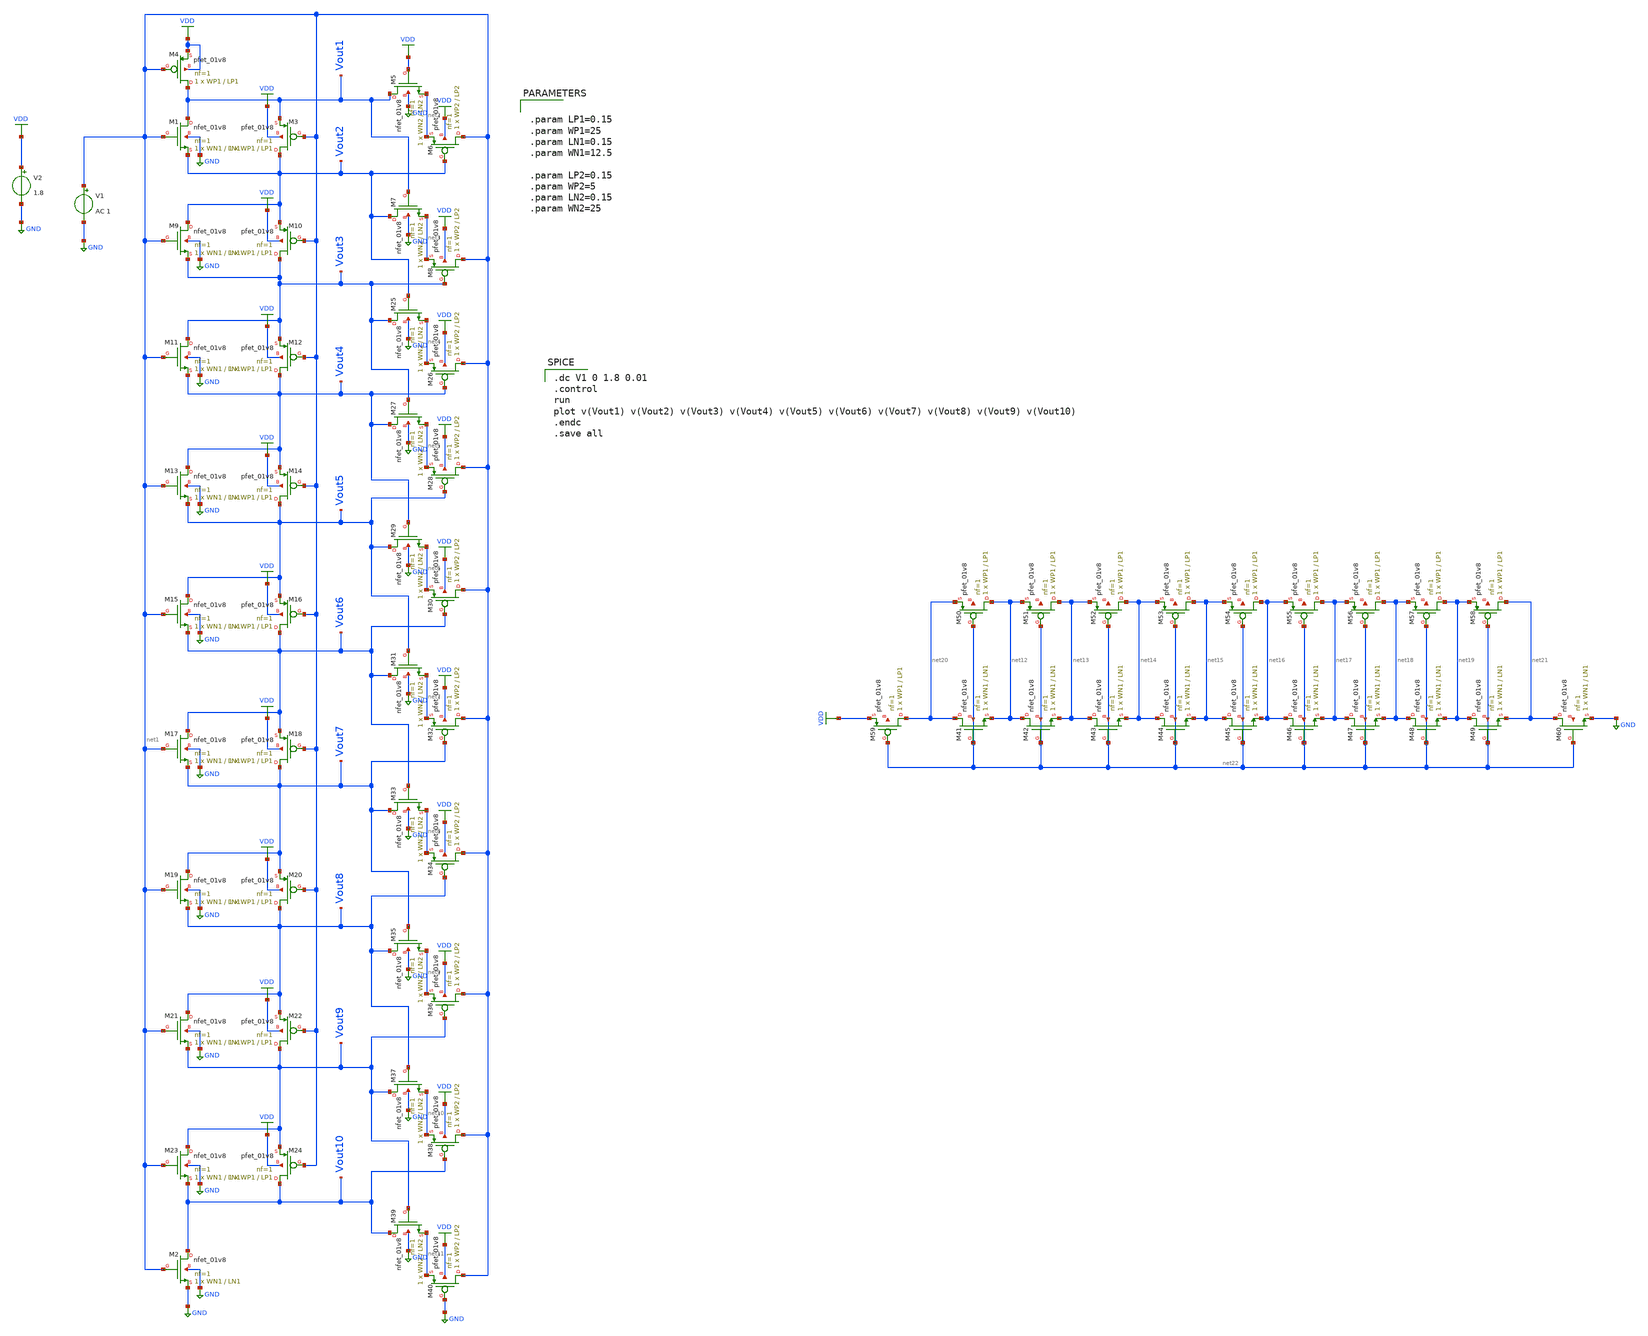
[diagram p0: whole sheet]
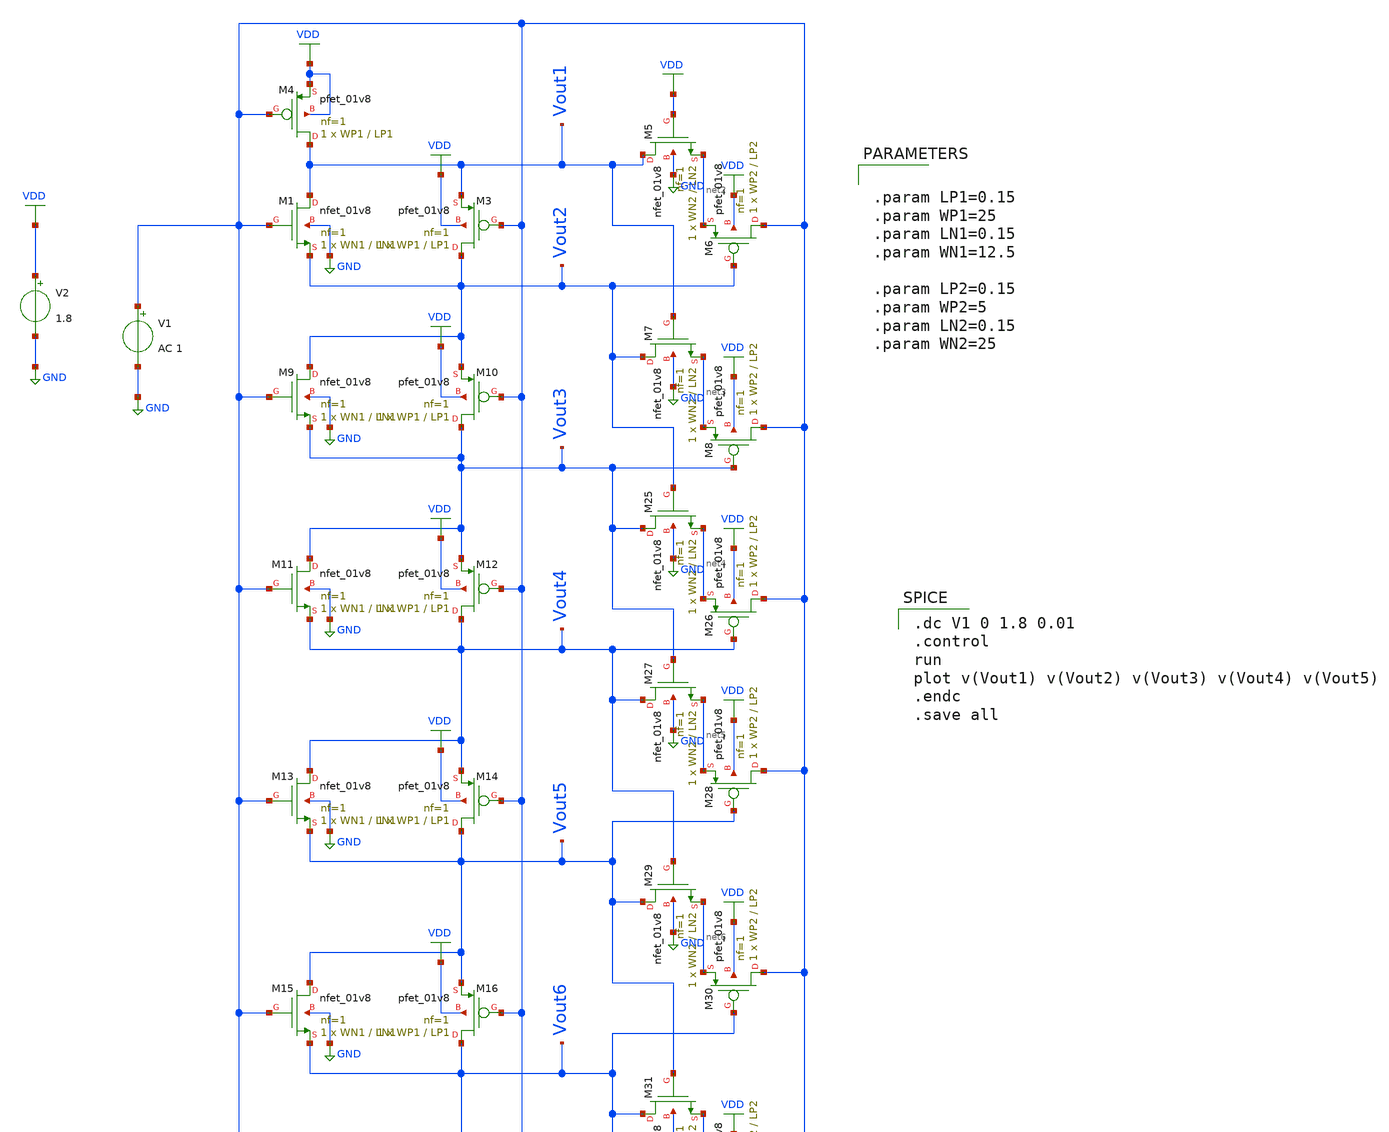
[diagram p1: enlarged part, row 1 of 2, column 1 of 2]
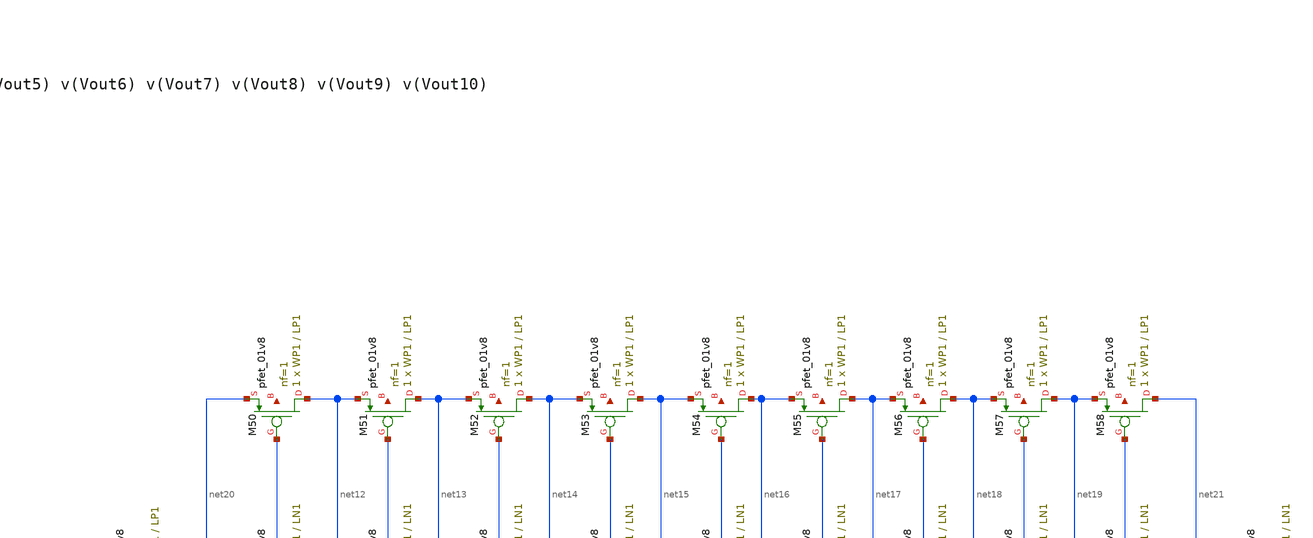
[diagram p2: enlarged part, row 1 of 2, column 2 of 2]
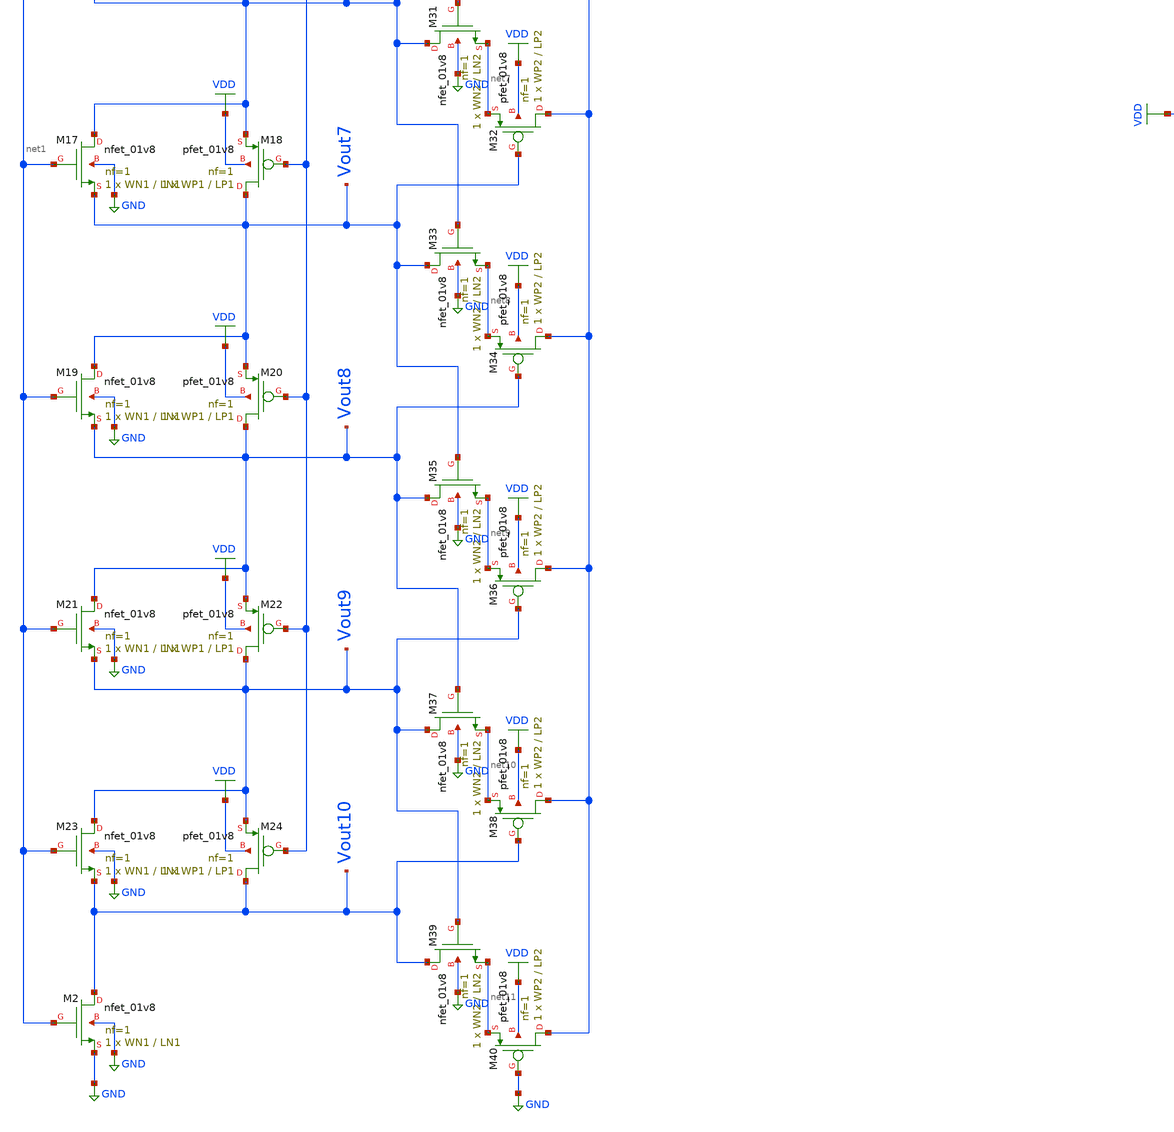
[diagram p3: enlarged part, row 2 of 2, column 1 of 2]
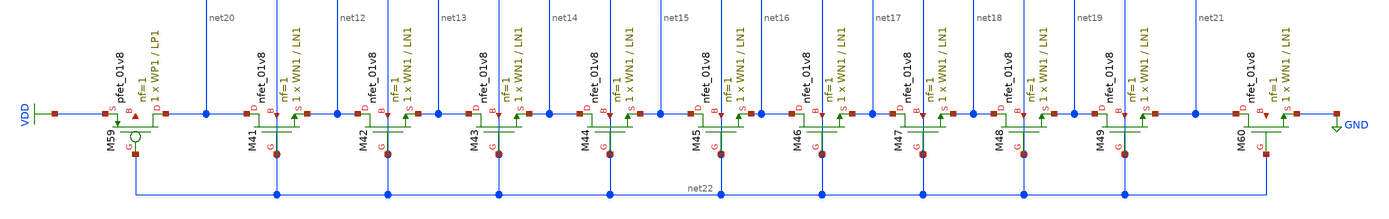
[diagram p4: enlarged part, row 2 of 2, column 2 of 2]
** sch_path: LIQAF circuit/10-Stage/10-stage LIQAF.sch
**.subckt 10-stage LIQAF
XM1 Vout1 net1 Vout2 GND sky130_fd_pr__nfet_01v8 L=LN1 W=WN1 nf=1 ad='int((nf+1)/2) * W/nf * 0.29' as='int((nf+2)/2) * W/nf * 0.29'
+ pd='2*int((nf+1)/2) * (W/nf + 0.29)' ps='2*int((nf+2)/2) * (W/nf + 0.29)' nrd='0.29 / W' nrs='0.29 / W'
+ sa=0 sb=0 sd=0 mult=1 m=1
V1 net1 GND AC 1
V2 VDD GND 1.8
XM2 Vout10 net1 GND GND sky130_fd_pr__nfet_01v8 L=LN1 W=WN1 nf=1 ad='int((nf+1)/2) * W/nf * 0.29' as='int((nf+2)/2) * W/nf * 0.29'
+ pd='2*int((nf+1)/2) * (W/nf + 0.29)' ps='2*int((nf+2)/2) * (W/nf + 0.29)' nrd='0.29 / W' nrs='0.29 / W'
+ sa=0 sb=0 sd=0 mult=1 m=1
XM3 Vout2 net1 Vout1 VDD sky130_fd_pr__pfet_01v8 L=LP1 W=WP1 nf=1 ad='int((nf+1)/2) * W/nf * 0.29' as='int((nf+2)/2) * W/nf * 0.29'
+ pd='2*int((nf+1)/2) * (W/nf + 0.29)' ps='2*int((nf+2)/2) * (W/nf + 0.29)' nrd='0.29 / W' nrs='0.29 / W'
+ sa=0 sb=0 sd=0 mult=1 m=1
XM4 Vout1 net1 VDD VDD sky130_fd_pr__pfet_01v8 L=LP1 W=WP1 nf=1 ad='int((nf+1)/2) * W/nf * 0.29' as='int((nf+2)/2) * W/nf * 0.29'
+ pd='2*int((nf+1)/2) * (W/nf + 0.29)' ps='2*int((nf+2)/2) * (W/nf + 0.29)' nrd='0.29 / W' nrs='0.29 / W'
+ sa=0 sb=0 sd=0 mult=1 m=1
XM5 Vout1 VDD net2 GND sky130_fd_pr__nfet_01v8 L=LN2 W=WN2 nf=1 ad='int((nf+1)/2) * W/nf * 0.29' as='int((nf+2)/2) * W/nf * 0.29'
+ pd='2*int((nf+1)/2) * (W/nf + 0.29)' ps='2*int((nf+2)/2) * (W/nf + 0.29)' nrd='0.29 / W' nrs='0.29 / W'
+ sa=0 sb=0 sd=0 mult=1 m=1
XM6 net1 Vout2 net2 VDD sky130_fd_pr__pfet_01v8 L=LP2 W=WP2 nf=1 ad='int((nf+1)/2) * W/nf * 0.29' as='int((nf+2)/2) * W/nf * 0.29'
+ pd='2*int((nf+1)/2) * (W/nf + 0.29)' ps='2*int((nf+2)/2) * (W/nf + 0.29)' nrd='0.29 / W' nrs='0.29 / W'
+ sa=0 sb=0 sd=0 mult=1 m=1
XM7 Vout2 Vout1 net3 GND sky130_fd_pr__nfet_01v8 L=LN2 W=WN2 nf=1 ad='int((nf+1)/2) * W/nf * 0.29' as='int((nf+2)/2) * W/nf * 0.29'
+ pd='2*int((nf+1)/2) * (W/nf + 0.29)' ps='2*int((nf+2)/2) * (W/nf + 0.29)' nrd='0.29 / W' nrs='0.29 / W'
+ sa=0 sb=0 sd=0 mult=1 m=1
XM8 net1 Vout3 net3 VDD sky130_fd_pr__pfet_01v8 L=LP2 W=WP2 nf=1 ad='int((nf+1)/2) * W/nf * 0.29' as='int((nf+2)/2) * W/nf * 0.29'
+ pd='2*int((nf+1)/2) * (W/nf + 0.29)' ps='2*int((nf+2)/2) * (W/nf + 0.29)' nrd='0.29 / W' nrs='0.29 / W'
+ sa=0 sb=0 sd=0 mult=1 m=1
XM9 Vout2 net1 Vout3 GND sky130_fd_pr__nfet_01v8 L=LN1 W=WN1 nf=1 ad='int((nf+1)/2) * W/nf * 0.29' as='int((nf+2)/2) * W/nf * 0.29'
+ pd='2*int((nf+1)/2) * (W/nf + 0.29)' ps='2*int((nf+2)/2) * (W/nf + 0.29)' nrd='0.29 / W' nrs='0.29 / W'
+ sa=0 sb=0 sd=0 mult=1 m=1
XM10 Vout3 net1 Vout2 VDD sky130_fd_pr__pfet_01v8 L=LP1 W=WP1 nf=1 ad='int((nf+1)/2) * W/nf * 0.29' as='int((nf+2)/2) * W/nf * 0.29'
+ pd='2*int((nf+1)/2) * (W/nf + 0.29)' ps='2*int((nf+2)/2) * (W/nf + 0.29)' nrd='0.29 / W' nrs='0.29 / W'
+ sa=0 sb=0 sd=0 mult=1 m=1
XM11 Vout3 net1 Vout4 GND sky130_fd_pr__nfet_01v8 L=LN1 W=WN1 nf=1 ad='int((nf+1)/2) * W/nf * 0.29' as='int((nf+2)/2) * W/nf * 0.29'
+ pd='2*int((nf+1)/2) * (W/nf + 0.29)' ps='2*int((nf+2)/2) * (W/nf + 0.29)' nrd='0.29 / W' nrs='0.29 / W'
+ sa=0 sb=0 sd=0 mult=1 m=1
XM12 Vout4 net1 Vout3 VDD sky130_fd_pr__pfet_01v8 L=LP1 W=WP1 nf=1 ad='int((nf+1)/2) * W/nf * 0.29' as='int((nf+2)/2) * W/nf * 0.29'
+ pd='2*int((nf+1)/2) * (W/nf + 0.29)' ps='2*int((nf+2)/2) * (W/nf + 0.29)' nrd='0.29 / W' nrs='0.29 / W'
+ sa=0 sb=0 sd=0 mult=1 m=1
XM13 Vout4 net1 Vout5 GND sky130_fd_pr__nfet_01v8 L=LN1 W=WN1 nf=1 ad='int((nf+1)/2) * W/nf * 0.29' as='int((nf+2)/2) * W/nf * 0.29'
+ pd='2*int((nf+1)/2) * (W/nf + 0.29)' ps='2*int((nf+2)/2) * (W/nf + 0.29)' nrd='0.29 / W' nrs='0.29 / W'
+ sa=0 sb=0 sd=0 mult=1 m=1
XM14 Vout5 net1 Vout4 VDD sky130_fd_pr__pfet_01v8 L=LP1 W=WP1 nf=1 ad='int((nf+1)/2) * W/nf * 0.29' as='int((nf+2)/2) * W/nf * 0.29'
+ pd='2*int((nf+1)/2) * (W/nf + 0.29)' ps='2*int((nf+2)/2) * (W/nf + 0.29)' nrd='0.29 / W' nrs='0.29 / W'
+ sa=0 sb=0 sd=0 mult=1 m=1
XM15 Vout5 net1 Vout6 GND sky130_fd_pr__nfet_01v8 L=LN1 W=WN1 nf=1 ad='int((nf+1)/2) * W/nf * 0.29' as='int((nf+2)/2) * W/nf * 0.29'
+ pd='2*int((nf+1)/2) * (W/nf + 0.29)' ps='2*int((nf+2)/2) * (W/nf + 0.29)' nrd='0.29 / W' nrs='0.29 / W'
+ sa=0 sb=0 sd=0 mult=1 m=1
XM16 Vout6 net1 Vout5 VDD sky130_fd_pr__pfet_01v8 L=LP1 W=WP1 nf=1 ad='int((nf+1)/2) * W/nf * 0.29' as='int((nf+2)/2) * W/nf * 0.29'
+ pd='2*int((nf+1)/2) * (W/nf + 0.29)' ps='2*int((nf+2)/2) * (W/nf + 0.29)' nrd='0.29 / W' nrs='0.29 / W'
+ sa=0 sb=0 sd=0 mult=1 m=1
XM17 Vout6 net1 Vout7 GND sky130_fd_pr__nfet_01v8 L=LN1 W=WN1 nf=1 ad='int((nf+1)/2) * W/nf * 0.29' as='int((nf+2)/2) * W/nf * 0.29'
+ pd='2*int((nf+1)/2) * (W/nf + 0.29)' ps='2*int((nf+2)/2) * (W/nf + 0.29)' nrd='0.29 / W' nrs='0.29 / W'
+ sa=0 sb=0 sd=0 mult=1 m=1
XM18 Vout7 net1 Vout6 VDD sky130_fd_pr__pfet_01v8 L=LP1 W=WP1 nf=1 ad='int((nf+1)/2) * W/nf * 0.29' as='int((nf+2)/2) * W/nf * 0.29'
+ pd='2*int((nf+1)/2) * (W/nf + 0.29)' ps='2*int((nf+2)/2) * (W/nf + 0.29)' nrd='0.29 / W' nrs='0.29 / W'
+ sa=0 sb=0 sd=0 mult=1 m=1
XM19 Vout7 net1 Vout8 GND sky130_fd_pr__nfet_01v8 L=LN1 W=WN1 nf=1 ad='int((nf+1)/2) * W/nf * 0.29' as='int((nf+2)/2) * W/nf * 0.29'
+ pd='2*int((nf+1)/2) * (W/nf + 0.29)' ps='2*int((nf+2)/2) * (W/nf + 0.29)' nrd='0.29 / W' nrs='0.29 / W'
+ sa=0 sb=0 sd=0 mult=1 m=1
XM20 Vout8 net1 Vout7 VDD sky130_fd_pr__pfet_01v8 L=LP1 W=WP1 nf=1 ad='int((nf+1)/2) * W/nf * 0.29' as='int((nf+2)/2) * W/nf * 0.29'
+ pd='2*int((nf+1)/2) * (W/nf + 0.29)' ps='2*int((nf+2)/2) * (W/nf + 0.29)' nrd='0.29 / W' nrs='0.29 / W'
+ sa=0 sb=0 sd=0 mult=1 m=1
XM21 Vout8 net1 Vout9 GND sky130_fd_pr__nfet_01v8 L=LN1 W=WN1 nf=1 ad='int((nf+1)/2) * W/nf * 0.29' as='int((nf+2)/2) * W/nf * 0.29'
+ pd='2*int((nf+1)/2) * (W/nf + 0.29)' ps='2*int((nf+2)/2) * (W/nf + 0.29)' nrd='0.29 / W' nrs='0.29 / W'
+ sa=0 sb=0 sd=0 mult=1 m=1
XM22 Vout9 net1 Vout8 VDD sky130_fd_pr__pfet_01v8 L=LP1 W=WP1 nf=1 ad='int((nf+1)/2) * W/nf * 0.29' as='int((nf+2)/2) * W/nf * 0.29'
+ pd='2*int((nf+1)/2) * (W/nf + 0.29)' ps='2*int((nf+2)/2) * (W/nf + 0.29)' nrd='0.29 / W' nrs='0.29 / W'
+ sa=0 sb=0 sd=0 mult=1 m=1
XM23 Vout9 net1 Vout10 GND sky130_fd_pr__nfet_01v8 L=LN1 W=WN1 nf=1 ad='int((nf+1)/2) * W/nf * 0.29'
+ as='int((nf+2)/2) * W/nf * 0.29' pd='2*int((nf+1)/2) * (W/nf + 0.29)' ps='2*int((nf+2)/2) * (W/nf + 0.29)'
+ nrd='0.29 / W' nrs='0.29 / W' sa=0 sb=0 sd=0 mult=1 m=1
XM24 Vout10 net1 Vout9 VDD sky130_fd_pr__pfet_01v8 L=LP1 W=WP1 nf=1 ad='int((nf+1)/2) * W/nf * 0.29'
+ as='int((nf+2)/2) * W/nf * 0.29' pd='2*int((nf+1)/2) * (W/nf + 0.29)' ps='2*int((nf+2)/2) * (W/nf + 0.29)'
+ nrd='0.29 / W' nrs='0.29 / W' sa=0 sb=0 sd=0 mult=1 m=1
XM25 Vout3 Vout2 net4 GND sky130_fd_pr__nfet_01v8 L=LN2 W=WN2 nf=1 ad='int((nf+1)/2) * W/nf * 0.29' as='int((nf+2)/2) * W/nf * 0.29'
+ pd='2*int((nf+1)/2) * (W/nf + 0.29)' ps='2*int((nf+2)/2) * (W/nf + 0.29)' nrd='0.29 / W' nrs='0.29 / W'
+ sa=0 sb=0 sd=0 mult=1 m=1
XM26 net1 Vout4 net4 VDD sky130_fd_pr__pfet_01v8 L=LP2 W=WP2 nf=1 ad='int((nf+1)/2) * W/nf * 0.29' as='int((nf+2)/2) * W/nf * 0.29'
+ pd='2*int((nf+1)/2) * (W/nf + 0.29)' ps='2*int((nf+2)/2) * (W/nf + 0.29)' nrd='0.29 / W' nrs='0.29 / W'
+ sa=0 sb=0 sd=0 mult=1 m=1
XM27 Vout4 Vout3 net5 GND sky130_fd_pr__nfet_01v8 L=LN2 W=WN2 nf=1 ad='int((nf+1)/2) * W/nf * 0.29' as='int((nf+2)/2) * W/nf * 0.29'
+ pd='2*int((nf+1)/2) * (W/nf + 0.29)' ps='2*int((nf+2)/2) * (W/nf + 0.29)' nrd='0.29 / W' nrs='0.29 / W'
+ sa=0 sb=0 sd=0 mult=1 m=1
XM28 net1 Vout5 net5 VDD sky130_fd_pr__pfet_01v8 L=LP2 W=WP2 nf=1 ad='int((nf+1)/2) * W/nf * 0.29' as='int((nf+2)/2) * W/nf * 0.29'
+ pd='2*int((nf+1)/2) * (W/nf + 0.29)' ps='2*int((nf+2)/2) * (W/nf + 0.29)' nrd='0.29 / W' nrs='0.29 / W'
+ sa=0 sb=0 sd=0 mult=1 m=1
XM29 Vout5 Vout4 net6 GND sky130_fd_pr__nfet_01v8 L=LN2 W=WN2 nf=1 ad='int((nf+1)/2) * W/nf * 0.29' as='int((nf+2)/2) * W/nf * 0.29'
+ pd='2*int((nf+1)/2) * (W/nf + 0.29)' ps='2*int((nf+2)/2) * (W/nf + 0.29)' nrd='0.29 / W' nrs='0.29 / W'
+ sa=0 sb=0 sd=0 mult=1 m=1
XM30 net1 Vout6 net6 VDD sky130_fd_pr__pfet_01v8 L=LP2 W=WP2 nf=1 ad='int((nf+1)/2) * W/nf * 0.29' as='int((nf+2)/2) * W/nf * 0.29'
+ pd='2*int((nf+1)/2) * (W/nf + 0.29)' ps='2*int((nf+2)/2) * (W/nf + 0.29)' nrd='0.29 / W' nrs='0.29 / W'
+ sa=0 sb=0 sd=0 mult=1 m=1
XM31 Vout6 Vout5 net7 GND sky130_fd_pr__nfet_01v8 L=LN2 W=WN2 nf=1 ad='int((nf+1)/2) * W/nf * 0.29' as='int((nf+2)/2) * W/nf * 0.29'
+ pd='2*int((nf+1)/2) * (W/nf + 0.29)' ps='2*int((nf+2)/2) * (W/nf + 0.29)' nrd='0.29 / W' nrs='0.29 / W'
+ sa=0 sb=0 sd=0 mult=1 m=1
XM32 net1 Vout7 net7 VDD sky130_fd_pr__pfet_01v8 L=LP2 W=WP2 nf=1 ad='int((nf+1)/2) * W/nf * 0.29' as='int((nf+2)/2) * W/nf * 0.29'
+ pd='2*int((nf+1)/2) * (W/nf + 0.29)' ps='2*int((nf+2)/2) * (W/nf + 0.29)' nrd='0.29 / W' nrs='0.29 / W'
+ sa=0 sb=0 sd=0 mult=1 m=1
XM33 Vout7 Vout6 net8 GND sky130_fd_pr__nfet_01v8 L=LN2 W=WN2 nf=1 ad='int((nf+1)/2) * W/nf * 0.29' as='int((nf+2)/2) * W/nf * 0.29'
+ pd='2*int((nf+1)/2) * (W/nf + 0.29)' ps='2*int((nf+2)/2) * (W/nf + 0.29)' nrd='0.29 / W' nrs='0.29 / W'
+ sa=0 sb=0 sd=0 mult=1 m=1
XM34 net1 Vout8 net8 VDD sky130_fd_pr__pfet_01v8 L=LP2 W=WP2 nf=1 ad='int((nf+1)/2) * W/nf * 0.29' as='int((nf+2)/2) * W/nf * 0.29'
+ pd='2*int((nf+1)/2) * (W/nf + 0.29)' ps='2*int((nf+2)/2) * (W/nf + 0.29)' nrd='0.29 / W' nrs='0.29 / W'
+ sa=0 sb=0 sd=0 mult=1 m=1
XM35 Vout8 Vout7 net9 GND sky130_fd_pr__nfet_01v8 L=LN2 W=WN2 nf=1 ad='int((nf+1)/2) * W/nf * 0.29' as='int((nf+2)/2) * W/nf * 0.29'
+ pd='2*int((nf+1)/2) * (W/nf + 0.29)' ps='2*int((nf+2)/2) * (W/nf + 0.29)' nrd='0.29 / W' nrs='0.29 / W'
+ sa=0 sb=0 sd=0 mult=1 m=1
XM36 net1 Vout9 net9 VDD sky130_fd_pr__pfet_01v8 L=LP2 W=WP2 nf=1 ad='int((nf+1)/2) * W/nf * 0.29' as='int((nf+2)/2) * W/nf * 0.29'
+ pd='2*int((nf+1)/2) * (W/nf + 0.29)' ps='2*int((nf+2)/2) * (W/nf + 0.29)' nrd='0.29 / W' nrs='0.29 / W'
+ sa=0 sb=0 sd=0 mult=1 m=1
XM37 Vout9 Vout8 net10 GND sky130_fd_pr__nfet_01v8 L=LN2 W=WN2 nf=1 ad='int((nf+1)/2) * W/nf * 0.29'
+ as='int((nf+2)/2) * W/nf * 0.29' pd='2*int((nf+1)/2) * (W/nf + 0.29)' ps='2*int((nf+2)/2) * (W/nf + 0.29)'
+ nrd='0.29 / W' nrs='0.29 / W' sa=0 sb=0 sd=0 mult=1 m=1
XM38 net1 Vout10 net10 VDD sky130_fd_pr__pfet_01v8 L=LP2 W=WP2 nf=1 ad='int((nf+1)/2) * W/nf * 0.29'
+ as='int((nf+2)/2) * W/nf * 0.29' pd='2*int((nf+1)/2) * (W/nf + 0.29)' ps='2*int((nf+2)/2) * (W/nf + 0.29)'
+ nrd='0.29 / W' nrs='0.29 / W' sa=0 sb=0 sd=0 mult=1 m=1
XM39 Vout10 Vout9 net11 GND sky130_fd_pr__nfet_01v8 L=LN2 W=WN2 nf=1 ad='int((nf+1)/2) * W/nf * 0.29'
+ as='int((nf+2)/2) * W/nf * 0.29' pd='2*int((nf+1)/2) * (W/nf + 0.29)' ps='2*int((nf+2)/2) * (W/nf + 0.29)'
+ nrd='0.29 / W' nrs='0.29 / W' sa=0 sb=0 sd=0 mult=1 m=1
XM40 net1 GND net11 VDD sky130_fd_pr__pfet_01v8 L=LP2 W=WP2 nf=1 ad='int((nf+1)/2) * W/nf * 0.29' as='int((nf+2)/2) * W/nf * 0.29'
+ pd='2*int((nf+1)/2) * (W/nf + 0.29)' ps='2*int((nf+2)/2) * (W/nf + 0.29)' nrd='0.29 / W' nrs='0.29 / W'
+ sa=0 sb=0 sd=0 mult=1 m=1
XM41 net20 net22 net12 net22 sky130_fd_pr__nfet_01v8 L=LN1 W=WN1 nf=1 ad='int((nf+1)/2) * W/nf * 0.29'
+ as='int((nf+2)/2) * W/nf * 0.29' pd='2*int((nf+1)/2) * (W/nf + 0.29)' ps='2*int((nf+2)/2) * (W/nf + 0.29)'
+ nrd='0.29 / W' nrs='0.29 / W' sa=0 sb=0 sd=0 mult=1 m=1
XM42 net12 net22 net13 net22 sky130_fd_pr__nfet_01v8 L=LN1 W=WN1 nf=1 ad='int((nf+1)/2) * W/nf * 0.29'
+ as='int((nf+2)/2) * W/nf * 0.29' pd='2*int((nf+1)/2) * (W/nf + 0.29)' ps='2*int((nf+2)/2) * (W/nf + 0.29)'
+ nrd='0.29 / W' nrs='0.29 / W' sa=0 sb=0 sd=0 mult=1 m=1
XM43 net13 net22 net14 net22 sky130_fd_pr__nfet_01v8 L=LN1 W=WN1 nf=1 ad='int((nf+1)/2) * W/nf * 0.29'
+ as='int((nf+2)/2) * W/nf * 0.29' pd='2*int((nf+1)/2) * (W/nf + 0.29)' ps='2*int((nf+2)/2) * (W/nf + 0.29)'
+ nrd='0.29 / W' nrs='0.29 / W' sa=0 sb=0 sd=0 mult=1 m=1
XM44 net14 net22 net15 net22 sky130_fd_pr__nfet_01v8 L=LN1 W=WN1 nf=1 ad='int((nf+1)/2) * W/nf * 0.29'
+ as='int((nf+2)/2) * W/nf * 0.29' pd='2*int((nf+1)/2) * (W/nf + 0.29)' ps='2*int((nf+2)/2) * (W/nf + 0.29)'
+ nrd='0.29 / W' nrs='0.29 / W' sa=0 sb=0 sd=0 mult=1 m=1
XM45 net15 net22 net16 net22 sky130_fd_pr__nfet_01v8 L=LN1 W=WN1 nf=1 ad='int((nf+1)/2) * W/nf * 0.29'
+ as='int((nf+2)/2) * W/nf * 0.29' pd='2*int((nf+1)/2) * (W/nf + 0.29)' ps='2*int((nf+2)/2) * (W/nf + 0.29)'
+ nrd='0.29 / W' nrs='0.29 / W' sa=0 sb=0 sd=0 mult=1 m=1
XM46 net16 net22 net17 net22 sky130_fd_pr__nfet_01v8 L=LN1 W=WN1 nf=1 ad='int((nf+1)/2) * W/nf * 0.29'
+ as='int((nf+2)/2) * W/nf * 0.29' pd='2*int((nf+1)/2) * (W/nf + 0.29)' ps='2*int((nf+2)/2) * (W/nf + 0.29)'
+ nrd='0.29 / W' nrs='0.29 / W' sa=0 sb=0 sd=0 mult=1 m=1
XM47 net17 net22 net18 net22 sky130_fd_pr__nfet_01v8 L=LN1 W=WN1 nf=1 ad='int((nf+1)/2) * W/nf * 0.29'
+ as='int((nf+2)/2) * W/nf * 0.29' pd='2*int((nf+1)/2) * (W/nf + 0.29)' ps='2*int((nf+2)/2) * (W/nf + 0.29)'
+ nrd='0.29 / W' nrs='0.29 / W' sa=0 sb=0 sd=0 mult=1 m=1
XM48 net18 net22 net19 net22 sky130_fd_pr__nfet_01v8 L=LN1 W=WN1 nf=1 ad='int((nf+1)/2) * W/nf * 0.29'
+ as='int((nf+2)/2) * W/nf * 0.29' pd='2*int((nf+1)/2) * (W/nf + 0.29)' ps='2*int((nf+2)/2) * (W/nf + 0.29)'
+ nrd='0.29 / W' nrs='0.29 / W' sa=0 sb=0 sd=0 mult=1 m=1
XM49 net19 net22 net21 net22 sky130_fd_pr__nfet_01v8 L=LN1 W=WN1 nf=1 ad='int((nf+1)/2) * W/nf * 0.29'
+ as='int((nf+2)/2) * W/nf * 0.29' pd='2*int((nf+1)/2) * (W/nf + 0.29)' ps='2*int((nf+2)/2) * (W/nf + 0.29)'
+ nrd='0.29 / W' nrs='0.29 / W' sa=0 sb=0 sd=0 mult=1 m=1
XM50 net12 net22 net20 net23 sky130_fd_pr__pfet_01v8 L=LP1 W=WP1 nf=1 ad='int((nf+1)/2) * W/nf * 0.29'
+ as='int((nf+2)/2) * W/nf * 0.29' pd='2*int((nf+1)/2) * (W/nf + 0.29)' ps='2*int((nf+2)/2) * (W/nf + 0.29)'
+ nrd='0.29 / W' nrs='0.29 / W' sa=0 sb=0 sd=0 mult=1 m=1
XM51 net13 net22 net12 net24 sky130_fd_pr__pfet_01v8 L=LP1 W=WP1 nf=1 ad='int((nf+1)/2) * W/nf * 0.29'
+ as='int((nf+2)/2) * W/nf * 0.29' pd='2*int((nf+1)/2) * (W/nf + 0.29)' ps='2*int((nf+2)/2) * (W/nf + 0.29)'
+ nrd='0.29 / W' nrs='0.29 / W' sa=0 sb=0 sd=0 mult=1 m=1
XM52 net14 net22 net13 net25 sky130_fd_pr__pfet_01v8 L=LP1 W=WP1 nf=1 ad='int((nf+1)/2) * W/nf * 0.29'
+ as='int((nf+2)/2) * W/nf * 0.29' pd='2*int((nf+1)/2) * (W/nf + 0.29)' ps='2*int((nf+2)/2) * (W/nf + 0.29)'
+ nrd='0.29 / W' nrs='0.29 / W' sa=0 sb=0 sd=0 mult=1 m=1
XM53 net15 net22 net14 net26 sky130_fd_pr__pfet_01v8 L=LP1 W=WP1 nf=1 ad='int((nf+1)/2) * W/nf * 0.29'
+ as='int((nf+2)/2) * W/nf * 0.29' pd='2*int((nf+1)/2) * (W/nf + 0.29)' ps='2*int((nf+2)/2) * (W/nf + 0.29)'
+ nrd='0.29 / W' nrs='0.29 / W' sa=0 sb=0 sd=0 mult=1 m=1
XM54 net16 net22 net15 net27 sky130_fd_pr__pfet_01v8 L=LP1 W=WP1 nf=1 ad='int((nf+1)/2) * W/nf * 0.29'
+ as='int((nf+2)/2) * W/nf * 0.29' pd='2*int((nf+1)/2) * (W/nf + 0.29)' ps='2*int((nf+2)/2) * (W/nf + 0.29)'
+ nrd='0.29 / W' nrs='0.29 / W' sa=0 sb=0 sd=0 mult=1 m=1
XM55 net17 net22 net16 net28 sky130_fd_pr__pfet_01v8 L=LP1 W=WP1 nf=1 ad='int((nf+1)/2) * W/nf * 0.29'
+ as='int((nf+2)/2) * W/nf * 0.29' pd='2*int((nf+1)/2) * (W/nf + 0.29)' ps='2*int((nf+2)/2) * (W/nf + 0.29)'
+ nrd='0.29 / W' nrs='0.29 / W' sa=0 sb=0 sd=0 mult=1 m=1
XM56 net18 net22 net17 net29 sky130_fd_pr__pfet_01v8 L=LP1 W=WP1 nf=1 ad='int((nf+1)/2) * W/nf * 0.29'
+ as='int((nf+2)/2) * W/nf * 0.29' pd='2*int((nf+1)/2) * (W/nf + 0.29)' ps='2*int((nf+2)/2) * (W/nf + 0.29)'
+ nrd='0.29 / W' nrs='0.29 / W' sa=0 sb=0 sd=0 mult=1 m=1
XM57 net19 net22 net18 net30 sky130_fd_pr__pfet_01v8 L=LP1 W=WP1 nf=1 ad='int((nf+1)/2) * W/nf * 0.29'
+ as='int((nf+2)/2) * W/nf * 0.29' pd='2*int((nf+1)/2) * (W/nf + 0.29)' ps='2*int((nf+2)/2) * (W/nf + 0.29)'
+ nrd='0.29 / W' nrs='0.29 / W' sa=0 sb=0 sd=0 mult=1 m=1
XM58 net21 net22 net19 net31 sky130_fd_pr__pfet_01v8 L=LP1 W=WP1 nf=1 ad='int((nf+1)/2) * W/nf * 0.29'
+ as='int((nf+2)/2) * W/nf * 0.29' pd='2*int((nf+1)/2) * (W/nf + 0.29)' ps='2*int((nf+2)/2) * (W/nf + 0.29)'
+ nrd='0.29 / W' nrs='0.29 / W' sa=0 sb=0 sd=0 mult=1 m=1
XM59 net20 net22 VDD net32 sky130_fd_pr__pfet_01v8 L=LP1 W=WP1 nf=1 ad='int((nf+1)/2) * W/nf * 0.29'
+ as='int((nf+2)/2) * W/nf * 0.29' pd='2*int((nf+1)/2) * (W/nf + 0.29)' ps='2*int((nf+2)/2) * (W/nf + 0.29)'
+ nrd='0.29 / W' nrs='0.29 / W' sa=0 sb=0 sd=0 mult=1 m=1
XM60 net21 net22 GND net33 sky130_fd_pr__nfet_01v8 L=LN1 W=WN1 nf=1 ad='int((nf+1)/2) * W/nf * 0.29'
+ as='int((nf+2)/2) * W/nf * 0.29' pd='2*int((nf+1)/2) * (W/nf + 0.29)' ps='2*int((nf+2)/2) * (W/nf + 0.29)'
+ nrd='0.29 / W' nrs='0.29 / W' sa=0 sb=0 sd=0 mult=1 m=1
**** begin user architecture code
 ** manual skywater pdks install (with patches applied)
* .lib $::SKYWATER_MODELS/models/sky130.lib.spice tt

** opencircuitdesign pdks install
.lib $::SKYWATER_MODELS/sky130.lib.spice tt

.param mc_mm_switch=0
.param mc_pr_switch=0
.param LP1=0.15


.dc V1 0 1.8 0.01
.control
run
plot v(Vout1) v(Vout2) v(Vout3) v(Vout4) v(Vout5) v(Vout6) v(Vout7) v(Vout8) v(Vout9) v(Vout10)
.endc
.save all



.param LP1=0.15
.param WP1=25
.param LN1=0.15
.param WN1=12.5

.param LP2=0.15
.param WP2=5
.param LN2=0.15
.param WN2=25


**** end user architecture code
**.ends
.GLOBAL GND
.GLOBAL VDD
.end
